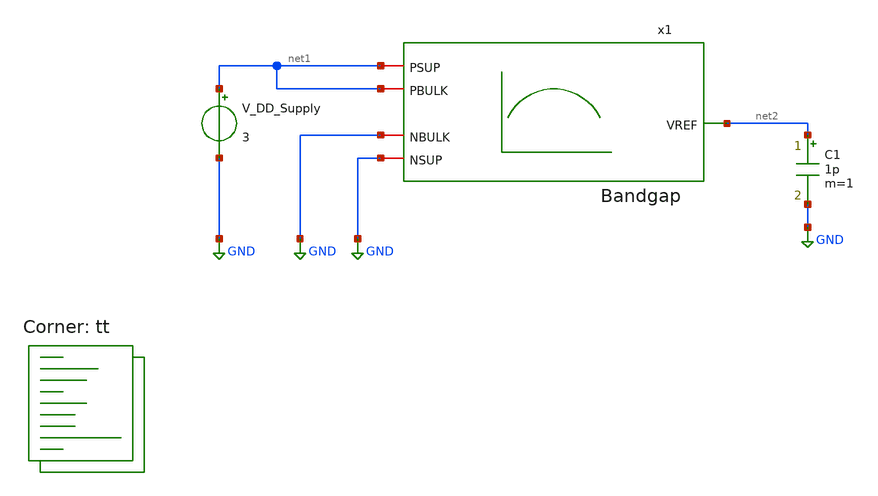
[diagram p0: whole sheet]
** sch_path: xschem/simulation_Bandgap_dcop.sch
**.subckt simulation_Bandgap_dcop
x1 net1 net1 net2 GND GND Bandgap
V_DD_Supply net1 GND 3
C1 net2 GND 1p m=1
**** begin user architecture code
.lib $::SKYWATER_MODELS/sky130.lib.spice tt
**** end user architecture code
**.ends

* expanding   symbol:  Bandgap.sym # of pins=5
** sym_path: xschem/Bandgap.sym
** sch_path: xschem/Bandgap.sch
.subckt Bandgap PSUP PBULK VREF NBULK NSUP
*.iopin PSUP
*.iopin NSUP
*.iopin NBULK
*.opin VREF
*.iopin PBULK
XM1 net1 net1 NSUP NBULK sky130_fd_pr__nfet_01v8 L=0.15 W=1 nf=1 ad='int((1 + 1)/2) * 1 / 1 * 0.29' as='int((1 + 2)/2) * 1 / 1 * 0.29'
+ pd='2*int((1 + 1)/2) * (1 / 1 + 0.29)' ps='2*int((1 + 2)/2) * (1 / 1 + 0.29)' nrd='0.29 / 1 ' nrs='0.29 / 1 '
+ sa=0 sb=0 sd=0 mult=50 m=50
XM2 net2 net2 NSUP NBULK sky130_fd_pr__nfet_01v8 L=0.55 W=1 nf=1 ad='int((1 + 1)/2) * 1 / 1 * 0.29' as='int((1 + 2)/2) * 1 / 1 * 0.29'
+ pd='2*int((1 + 1)/2) * (1 / 1 + 0.29)' ps='2*int((1 + 2)/2) * (1 / 1 + 0.29)' nrd='0.29 / 1 ' nrs='0.29 / 1 '
+ sa=0 sb=0 sd=0 mult=10 m=10
R1 net4 net1 1k m=1
R2 VREF net2 2k m=1
XM3 net3 net3 PSUP PBULK sky130_fd_pr__pfet_01v8 L=0.15 W=2 nf=1 ad='int((nf+1)/2) * W/nf * 0.29' as='int((nf+2)/2) * W/nf * 0.29'
+ pd='2*int((nf+1)/2) * (W/nf + 0.29)' ps='2*int((nf+2)/2) * (W/nf + 0.29)' nrd='0.29 / W' nrs='0.29 / W'
+ sa=0 sb=0 sd=0 mult=1 m=1
XM4 net5 net3 PSUP PBULK sky130_fd_pr__pfet_01v8 L=0.15 W=2 nf=1 ad='int((nf+1)/2) * W/nf * 0.29' as='int((nf+2)/2) * W/nf * 0.29'
+ pd='2*int((nf+1)/2) * (W/nf + 0.29)' ps='2*int((nf+2)/2) * (W/nf + 0.29)' nrd='0.29 / W' nrs='0.29 / W'
+ sa=0 sb=0 sd=0 mult=1 m=1
E1 net3 NSUP VREF net4 10000
VBE net3 net4 0
.save i(vbe)
VPTATCTAT net5 VREF 0
.save i(vptatctat)
XM5 net6 net3 PSUP PBULK sky130_fd_pr__pfet_01v8 L=0.15 W=2 nf=1 ad='int((nf+1)/2) * W/nf * 0.29' as='int((nf+2)/2) * W/nf * 0.29'
+ pd='2*int((nf+1)/2) * (W/nf + 0.29)' ps='2*int((nf+2)/2) * (W/nf + 0.29)' nrd='0.29 / W' nrs='0.29 / W'
+ sa=0 sb=0 sd=0 mult=1 m=1
R3 VREFOUT NSUP 1k m=1
VOUT net6 VREFOUT 0
.save i(vout)
.ends

.GLOBAL GND
**** begin user architecture code


* ngspice commands
.options savecurrents

.control
save all
save @m.x1.xm1.msky130_fd_pr__nfet_01v8[gm]
save @m.x1.xm1.msky130_fd_pr__nfet_01v8[gds]
save @m.x1.xm1.msky130_fd_pr__nfet_01v8[gmbs]
save @m.x1.xm1.msky130_fd_pr__nfet_01v8[vth]
save @m.x1.xm1.msky130_fd_pr__nfet_01v8[vgs]
save @m.x1.xm2.msky130_fd_pr__nfet_01v8[gm]
save @m.x1.xm2.msky130_fd_pr__nfet_01v8[gds]
save @m.x1.xm2.msky130_fd_pr__nfet_01v8[gmbs]
save @m.x1.xm2.msky130_fd_pr__nfet_01v8[vth]
save @m.x1.xm2.msky130_fd_pr__nfet_01v8[vgs]
*op
dc temp -20 140 10
print @m.x1.xm1.msky130_fd_pr__nfet_01v8[vth]
write simulate_Bandgap_dcop.raw
*quit 0
.endc



**** end user architecture code
.end
